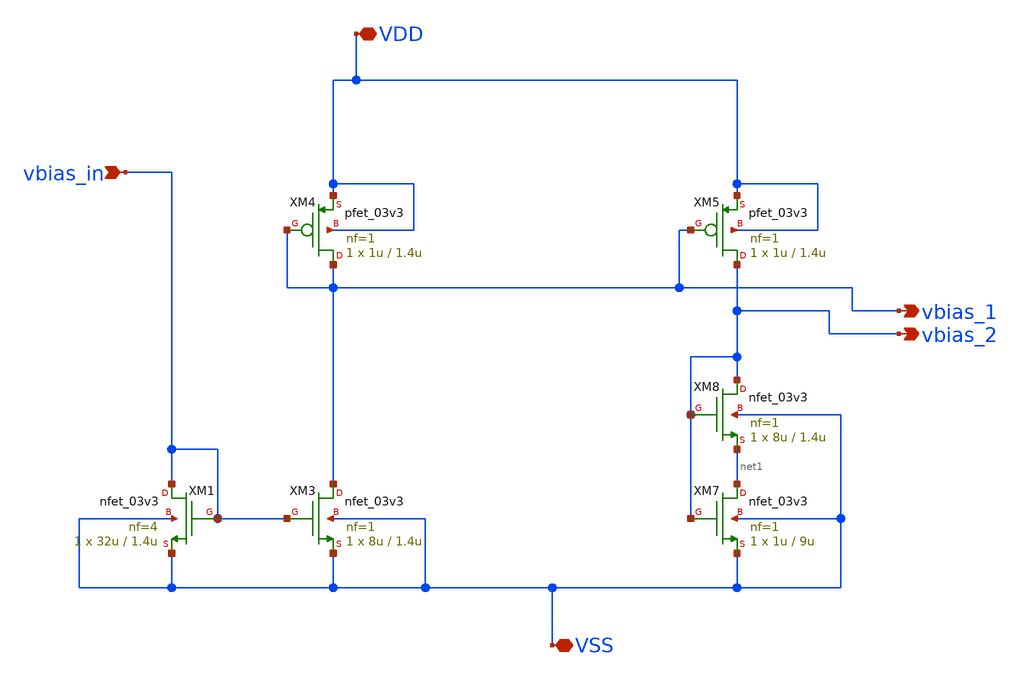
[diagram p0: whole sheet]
** sch_path: xschem/amp_bias.sch
**.subckt amp_bias VDD VSS vbias_1 vbias_2 vbias_in
*.iopin VDD
*.iopin VSS
*.opin vbias_1
*.opin vbias_2
*.ipin vbias_in
XM1 vbias_in vbias_in VSS VSS nfet_03v3 L=1.4u W=32u nf=4 ad='int((nf+1)/2) * W/nf * 0.18u' as='int((nf+2)/2) * W/nf * 0.18u'
+ pd='2*int((nf+1)/2) * (W/nf + 0.18u)' ps='2*int((nf+2)/2) * (W/nf + 0.18u)' nrd='0.18u / W' nrs='0.18u / W'
+ sa=0 sb=0 sd=0 m=1 par=1
XM3 vbias_1 vbias_in VSS VSS nfet_03v3 L=1.4u W=8u nf=1 ad='int((nf+1)/2) * W/nf * 0.18u' as='int((nf+2)/2) * W/nf * 0.18u'
+ pd='2*int((nf+1)/2) * (W/nf + 0.18u)' ps='2*int((nf+2)/2) * (W/nf + 0.18u)' nrd='0.18u / W' nrs='0.18u / W'
+ sa=0 sb=0 sd=0 m=1 par=1
XM4 vbias_1 vbias_1 VDD VDD pfet_03v3 L=1.4u W=1u nf=1 ad='int((nf+1)/2) * W/nf * 0.18u' as='int((nf+2)/2) * W/nf * 0.18u'
+ pd='2*int((nf+1)/2) * (W/nf + 0.18u)' ps='2*int((nf+2)/2) * (W/nf + 0.18u)' nrd='0.18u / W' nrs='0.18u / W'
+ sa=0 sb=0 sd=0 m=1
XM5 vbias_2 vbias_1 VDD VDD pfet_03v3 L=1.4u W=1u nf=1 ad='int((nf+1)/2) * W/nf * 0.18u' as='int((nf+2)/2) * W/nf * 0.18u'
+ pd='2*int((nf+1)/2) * (W/nf + 0.18u)' ps='2*int((nf+2)/2) * (W/nf + 0.18u)' nrd='0.18u / W' nrs='0.18u / W'
+ sa=0 sb=0 sd=0 m=1
XM7 net1 vbias_2 VSS VSS nfet_03v3 L=9u W=1u nf=1 ad='int((nf+1)/2) * W/nf * 0.18u' as='int((nf+2)/2) * W/nf * 0.18u'
+ pd='2*int((nf+1)/2) * (W/nf + 0.18u)' ps='2*int((nf+2)/2) * (W/nf + 0.18u)' nrd='0.18u / W' nrs='0.18u / W'
+ sa=0 sb=0 sd=0 m=1 par=1
XM8 vbias_2 vbias_2 net1 VSS nfet_03v3 L=1.4u W=8u nf=1 ad='int((nf+1)/2) * W/nf * 0.18u' as='int((nf+2)/2) * W/nf * 0.18u'
+ pd='2*int((nf+1)/2) * (W/nf + 0.18u)' ps='2*int((nf+2)/2) * (W/nf + 0.18u)' nrd='0.18u / W' nrs='0.18u / W'
+ sa=0 sb=0 sd=0 m=1 par=1
**.ends
.end
